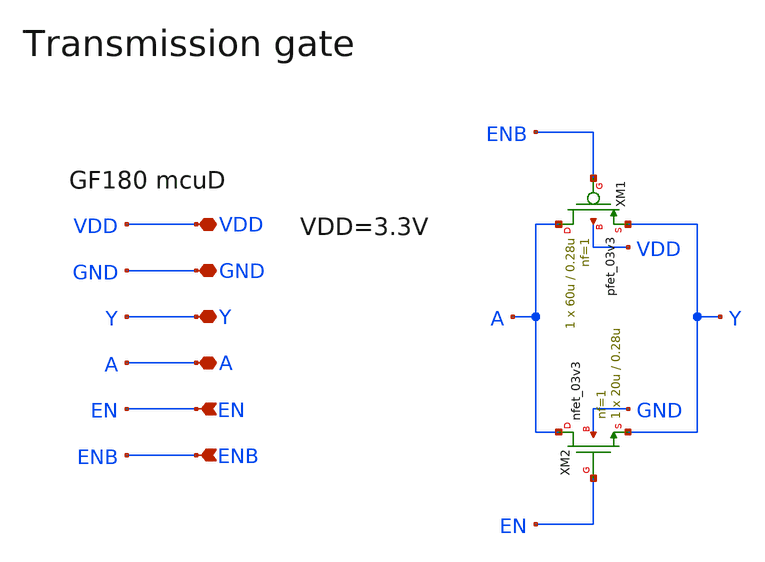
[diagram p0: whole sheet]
** sch_path: designs/libs/core_analog/trans_gate/trans_gate.sch
* Copyright 2022 GlobalFoundries PDK Authors
* Licensed under the Apache License, Version 2.0 (the "License");
* you may not use this file except in compliance with the License.
* You may obtain a copy of the License at
* https://www.apache.org/licenses/LICENSE-2.0
* Unless required by applicable law or agreed to in writing, software
* distributed under the License is distributed on an "AS IS" BASIS,
* WITHOUT WARRANTIES OR CONDITIONS OF ANY KIND, either express or implied.
* See the License for the specific language governing permissions and
* limitations under the License.
**.subckt trans_gate EN ENB VDD GND Y A
*.ipin EN
*.ipin ENB
*.iopin VDD
*.iopin GND
*.iopin Y
*.iopin A
XM1 A ENB Y VDD pfet_03v3 L=0.28u W=60u nf=1 ad='int((nf+1)/2) * W/nf * 0.18u' as='int((nf+2)/2) * W/nf * 0.18u'
+ pd='2*int((nf+1)/2) * (W/nf + 0.18u)' ps='2*int((nf+2)/2) * (W/nf + 0.18u)' nrd='0.18u / W' nrs='0.18u / W'
+ sa=0 sb=0 sd=0 m=1
XM2 A EN Y GND nfet_03v3 L=0.28u W=20u nf=1 ad='int((nf+1)/2) * W/nf * 0.18u' as='int((nf+2)/2) * W/nf * 0.18u'
+ pd='2*int((nf+1)/2) * (W/nf + 0.18u)' ps='2*int((nf+2)/2) * (W/nf + 0.18u)' nrd='0.18u / W' nrs='0.18u / W'
+ sa=0 sb=0 sd=0 m=1
**.ends
.end
